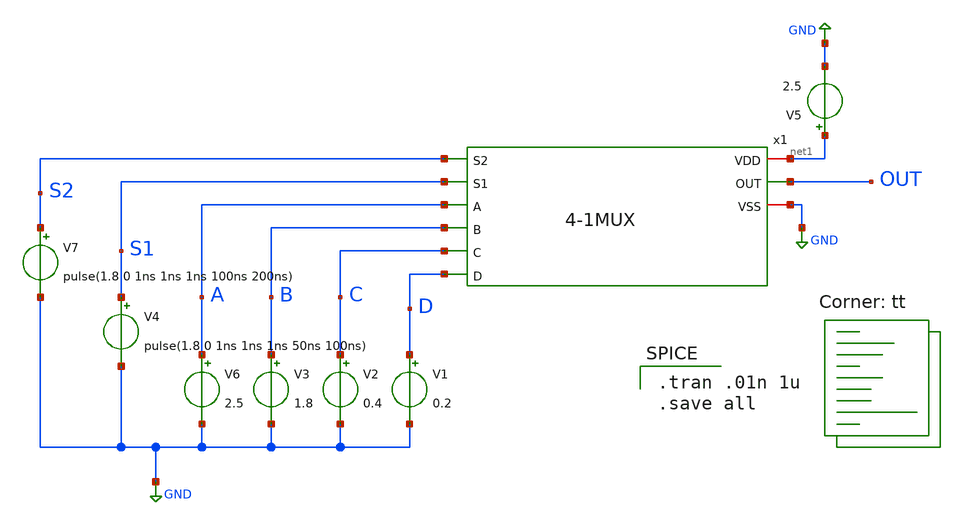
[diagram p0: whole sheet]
** sch_path: xschem/Testbenches/4-1MUXTB.sch
**.subckt 4-1MUXTB
x1 net1 S2 S1 A B OUT C D GND 4-1MUX
V5 net1 GND 2.5
V4 S1 GND pulse(1.8 0 1ns 1ns 1ns 50ns 100ns)
V1 D GND 0.2
V2 C GND 0.4
V3 B GND 1.8
V6 A GND 2.5
V7 S2 GND pulse(1.8 0 1ns 1ns 1ns 100ns 200ns)
**** begin user architecture code
.lib $::SKYWATER_MODELS/sky130.lib.spice tt

.tran .01n 1u
.save all

**** end user architecture code
**.ends
.GLOBAL GND
.end
